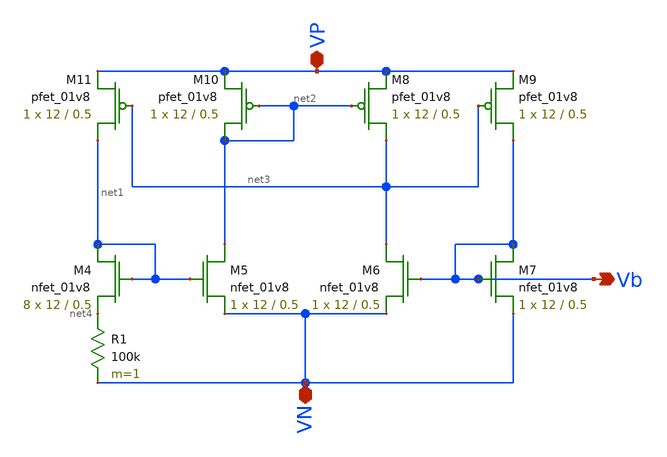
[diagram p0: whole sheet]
** sch_path: schematics/bias_3/current_bias.sch
**.subckt current_bias VP VN Vb
*.iopin VP
*.iopin VN
*.opin Vb
XM4 net1 net1 net4 GND sky130_fd_pr__nfet_01v8 L=0.5 W=12 nf=1 ad='int((nf+1)/2) * W/nf * 0.29' as='int((nf+2)/2) * W/nf * 0.29'
+ pd='2*int((nf+1)/2) * (W/nf + 0.29)' ps='2*int((nf+2)/2) * (W/nf + 0.29)' nrd='0.29 / W' nrs='0.29 / W'
+ sa=0 sb=0 sd=0 mult=8 m=8
XM5 net2 net1 VN GND sky130_fd_pr__nfet_01v8 L=0.5 W=12 nf=1 ad='int((nf+1)/2) * W/nf * 0.29' as='int((nf+2)/2) * W/nf * 0.29'
+ pd='2*int((nf+1)/2) * (W/nf + 0.29)' ps='2*int((nf+2)/2) * (W/nf + 0.29)' nrd='0.29 / W' nrs='0.29 / W'
+ sa=0 sb=0 sd=0 mult=1 m=1
XM6 net3 Vb VN GND sky130_fd_pr__nfet_01v8 L=0.5 W=12 nf=1 ad='int((nf+1)/2) * W/nf * 0.29' as='int((nf+2)/2) * W/nf * 0.29'
+ pd='2*int((nf+1)/2) * (W/nf + 0.29)' ps='2*int((nf+2)/2) * (W/nf + 0.29)' nrd='0.29 / W' nrs='0.29 / W'
+ sa=0 sb=0 sd=0 mult=1 m=1
XM7 Vb Vb VN GND sky130_fd_pr__nfet_01v8 L=0.5 W=12 nf=1 ad='int((nf+1)/2) * W/nf * 0.29' as='int((nf+2)/2) * W/nf * 0.29'
+ pd='2*int((nf+1)/2) * (W/nf + 0.29)' ps='2*int((nf+2)/2) * (W/nf + 0.29)' nrd='0.29 / W' nrs='0.29 / W'
+ sa=0 sb=0 sd=0 mult=1 m=1
R1 net4 VN 100k m=1
XM8 net3 net2 VP VDD sky130_fd_pr__pfet_01v8 L=0.5 W=12 nf=1 ad='int((nf+1)/2) * W/nf * 0.29' as='int((nf+2)/2) * W/nf * 0.29'
+ pd='2*int((nf+1)/2) * (W/nf + 0.29)' ps='2*int((nf+2)/2) * (W/nf + 0.29)' nrd='0.29 / W' nrs='0.29 / W'
+ sa=0 sb=0 sd=0 mult=1 m=1
XM9 Vb net3 VP VDD sky130_fd_pr__pfet_01v8 L=0.5 W=12 nf=1 ad='int((nf+1)/2) * W/nf * 0.29' as='int((nf+2)/2) * W/nf * 0.29'
+ pd='2*int((nf+1)/2) * (W/nf + 0.29)' ps='2*int((nf+2)/2) * (W/nf + 0.29)' nrd='0.29 / W' nrs='0.29 / W'
+ sa=0 sb=0 sd=0 mult=1 m=1
XM10 net2 net2 VP VDD sky130_fd_pr__pfet_01v8 L=0.5 W=12 nf=1 ad='int((nf+1)/2) * W/nf * 0.29' as='int((nf+2)/2) * W/nf * 0.29'
+ pd='2*int((nf+1)/2) * (W/nf + 0.29)' ps='2*int((nf+2)/2) * (W/nf + 0.29)' nrd='0.29 / W' nrs='0.29 / W'
+ sa=0 sb=0 sd=0 mult=1 m=1
XM11 net1 net3 VP VDD sky130_fd_pr__pfet_01v8 L=0.5 W=12 nf=1 ad='int((nf+1)/2) * W/nf * 0.29' as='int((nf+2)/2) * W/nf * 0.29'
+ pd='2*int((nf+1)/2) * (W/nf + 0.29)' ps='2*int((nf+2)/2) * (W/nf + 0.29)' nrd='0.29 / W' nrs='0.29 / W'
+ sa=0 sb=0 sd=0 mult=1 m=1
**.ends
.end
